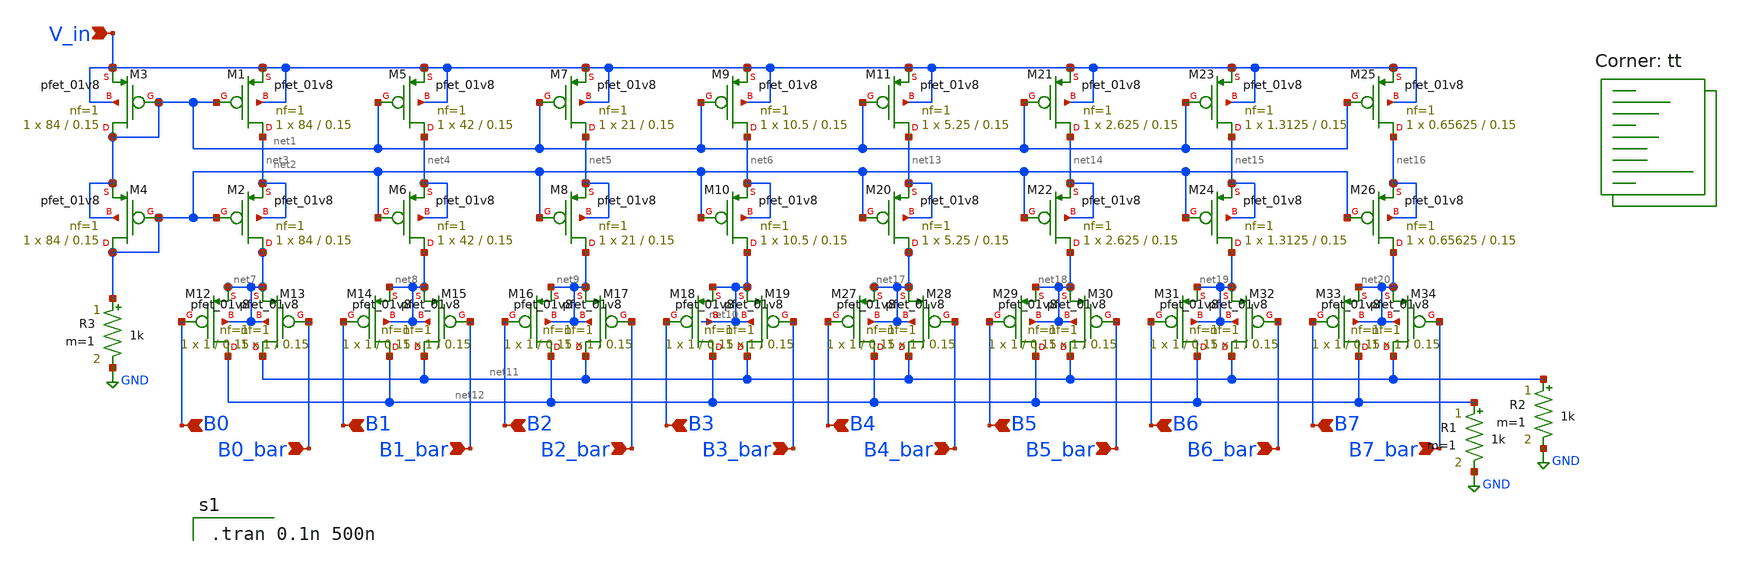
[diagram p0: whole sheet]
** sch_path: analog/schematics/DAC.sch
**.subckt DAC B0 V_in B0_bar B1 B2 B3 B1_bar B2_bar B3_bar B4 B4_bar B5 B6 B7 B5_bar B6_bar B7_bar
*.ipin B0
*.ipin V_in
*.ipin B0_bar
*.ipin B1
*.ipin B2
*.ipin B3
*.ipin B1_bar
*.ipin B2_bar
*.ipin B3_bar
*.ipin B4
*.ipin B4_bar
*.ipin B5
*.ipin B6
*.ipin B7
*.ipin B5_bar
*.ipin B6_bar
*.ipin B7_bar
XM1 net3 net1 V_in V_in sky130_fd_pr__pfet_01v8 L=0.15 W=84 nf=1 ad='int((nf+1)/2) * W/nf * 0.29' as='int((nf+2)/2) * W/nf * 0.29'
+ pd='2*int((nf+1)/2) * (W/nf + 0.29)' ps='2*int((nf+2)/2) * (W/nf + 0.29)' nrd='0.29 / W' nrs='0.29 / W'
+ sa=0 sb=0 sd=0 mult=1 m=1
XM2 net7 net2 net3 net3 sky130_fd_pr__pfet_01v8 L=0.15 W=84 nf=1 ad='int((nf+1)/2) * W/nf * 0.29' as='int((nf+2)/2) * W/nf * 0.29'
+ pd='2*int((nf+1)/2) * (W/nf + 0.29)' ps='2*int((nf+2)/2) * (W/nf + 0.29)' nrd='0.29 / W' nrs='0.29 / W'
+ sa=0 sb=0 sd=0 mult=1 m=1
XM3 net1 net1 V_in V_in sky130_fd_pr__pfet_01v8 L=0.15 W=84 nf=1 ad='int((nf+1)/2) * W/nf * 0.29' as='int((nf+2)/2) * W/nf * 0.29'
+ pd='2*int((nf+1)/2) * (W/nf + 0.29)' ps='2*int((nf+2)/2) * (W/nf + 0.29)' nrd='0.29 / W' nrs='0.29 / W'
+ sa=0 sb=0 sd=0 mult=1 m=1
XM4 net2 net2 net1 net1 sky130_fd_pr__pfet_01v8 L=0.15 W=84 nf=1 ad='int((nf+1)/2) * W/nf * 0.29' as='int((nf+2)/2) * W/nf * 0.29'
+ pd='2*int((nf+1)/2) * (W/nf + 0.29)' ps='2*int((nf+2)/2) * (W/nf + 0.29)' nrd='0.29 / W' nrs='0.29 / W'
+ sa=0 sb=0 sd=0 mult=1 m=1
XM5 net4 net1 V_in V_in sky130_fd_pr__pfet_01v8 L=0.15 W=42 nf=1 ad='int((nf+1)/2) * W/nf * 0.29' as='int((nf+2)/2) * W/nf * 0.29'
+ pd='2*int((nf+1)/2) * (W/nf + 0.29)' ps='2*int((nf+2)/2) * (W/nf + 0.29)' nrd='0.29 / W' nrs='0.29 / W'
+ sa=0 sb=0 sd=0 mult=1 m=1
XM6 net8 net2 net4 net4 sky130_fd_pr__pfet_01v8 L=0.15 W=42 nf=1 ad='int((nf+1)/2) * W/nf * 0.29' as='int((nf+2)/2) * W/nf * 0.29'
+ pd='2*int((nf+1)/2) * (W/nf + 0.29)' ps='2*int((nf+2)/2) * (W/nf + 0.29)' nrd='0.29 / W' nrs='0.29 / W'
+ sa=0 sb=0 sd=0 mult=1 m=1
XM7 net5 net1 V_in V_in sky130_fd_pr__pfet_01v8 L=0.15 W=21 nf=1 ad='int((nf+1)/2) * W/nf * 0.29' as='int((nf+2)/2) * W/nf * 0.29'
+ pd='2*int((nf+1)/2) * (W/nf + 0.29)' ps='2*int((nf+2)/2) * (W/nf + 0.29)' nrd='0.29 / W' nrs='0.29 / W'
+ sa=0 sb=0 sd=0 mult=1 m=1
XM8 net9 net2 net5 net5 sky130_fd_pr__pfet_01v8 L=0.15 W=21 nf=1 ad='int((nf+1)/2) * W/nf * 0.29' as='int((nf+2)/2) * W/nf * 0.29'
+ pd='2*int((nf+1)/2) * (W/nf + 0.29)' ps='2*int((nf+2)/2) * (W/nf + 0.29)' nrd='0.29 / W' nrs='0.29 / W'
+ sa=0 sb=0 sd=0 mult=1 m=1
XM9 net6 net1 V_in V_in sky130_fd_pr__pfet_01v8 L=0.15 W=10.5 nf=1 ad='int((nf+1)/2) * W/nf * 0.29' as='int((nf+2)/2) * W/nf * 0.29'
+ pd='2*int((nf+1)/2) * (W/nf + 0.29)' ps='2*int((nf+2)/2) * (W/nf + 0.29)' nrd='0.29 / W' nrs='0.29 / W'
+ sa=0 sb=0 sd=0 mult=1 m=1
XM10 net10 net2 net6 net6 sky130_fd_pr__pfet_01v8 L=0.15 W=10.5 nf=1 ad='int((nf+1)/2) * W/nf * 0.29'
+ as='int((nf+2)/2) * W/nf * 0.29' pd='2*int((nf+1)/2) * (W/nf + 0.29)' ps='2*int((nf+2)/2) * (W/nf + 0.29)'
+ nrd='0.29 / W' nrs='0.29 / W' sa=0 sb=0 sd=0 mult=1 m=1
XM12 net12 B0 net7 net7 sky130_fd_pr__pfet_01v8 L=0.15 W=1 nf=1 ad='int((nf+1)/2) * W/nf * 0.29' as='int((nf+2)/2) * W/nf * 0.29'
+ pd='2*int((nf+1)/2) * (W/nf + 0.29)' ps='2*int((nf+2)/2) * (W/nf + 0.29)' nrd='0.29 / W' nrs='0.29 / W'
+ sa=0 sb=0 sd=0 mult=1 m=1
XM13 net11 B0_bar net7 net7 sky130_fd_pr__pfet_01v8 L=0.15 W=1 nf=1 ad='int((nf+1)/2) * W/nf * 0.29'
+ as='int((nf+2)/2) * W/nf * 0.29' pd='2*int((nf+1)/2) * (W/nf + 0.29)' ps='2*int((nf+2)/2) * (W/nf + 0.29)'
+ nrd='0.29 / W' nrs='0.29 / W' sa=0 sb=0 sd=0 mult=1 m=1
XM14 net12 B1 net8 net8 sky130_fd_pr__pfet_01v8 L=0.15 W=1 nf=1 ad='int((nf+1)/2) * W/nf * 0.29' as='int((nf+2)/2) * W/nf * 0.29'
+ pd='2*int((nf+1)/2) * (W/nf + 0.29)' ps='2*int((nf+2)/2) * (W/nf + 0.29)' nrd='0.29 / W' nrs='0.29 / W'
+ sa=0 sb=0 sd=0 mult=1 m=1
XM15 net11 B1_bar net8 net8 sky130_fd_pr__pfet_01v8 L=0.15 W=1 nf=1 ad='int((nf+1)/2) * W/nf * 0.29'
+ as='int((nf+2)/2) * W/nf * 0.29' pd='2*int((nf+1)/2) * (W/nf + 0.29)' ps='2*int((nf+2)/2) * (W/nf + 0.29)'
+ nrd='0.29 / W' nrs='0.29 / W' sa=0 sb=0 sd=0 mult=1 m=1
XM16 net12 B2 net9 net9 sky130_fd_pr__pfet_01v8 L=0.15 W=1 nf=1 ad='int((nf+1)/2) * W/nf * 0.29' as='int((nf+2)/2) * W/nf * 0.29'
+ pd='2*int((nf+1)/2) * (W/nf + 0.29)' ps='2*int((nf+2)/2) * (W/nf + 0.29)' nrd='0.29 / W' nrs='0.29 / W'
+ sa=0 sb=0 sd=0 mult=1 m=1
XM17 net11 B2_bar net9 net9 sky130_fd_pr__pfet_01v8 L=0.15 W=1 nf=1 ad='int((nf+1)/2) * W/nf * 0.29'
+ as='int((nf+2)/2) * W/nf * 0.29' pd='2*int((nf+1)/2) * (W/nf + 0.29)' ps='2*int((nf+2)/2) * (W/nf + 0.29)'
+ nrd='0.29 / W' nrs='0.29 / W' sa=0 sb=0 sd=0 mult=1 m=1
XM18 net12 B3 net10 net10 sky130_fd_pr__pfet_01v8 L=0.15 W=1 nf=1 ad='int((nf+1)/2) * W/nf * 0.29' as='int((nf+2)/2) * W/nf * 0.29'
+ pd='2*int((nf+1)/2) * (W/nf + 0.29)' ps='2*int((nf+2)/2) * (W/nf + 0.29)' nrd='0.29 / W' nrs='0.29 / W'
+ sa=0 sb=0 sd=0 mult=1 m=1
XM19 net11 B3_bar net10 net10 sky130_fd_pr__pfet_01v8 L=0.15 W=1 nf=1 ad='int((nf+1)/2) * W/nf * 0.29'
+ as='int((nf+2)/2) * W/nf * 0.29' pd='2*int((nf+1)/2) * (W/nf + 0.29)' ps='2*int((nf+2)/2) * (W/nf + 0.29)'
+ nrd='0.29 / W' nrs='0.29 / W' sa=0 sb=0 sd=0 mult=1 m=1
XM11 net13 net1 V_in V_in sky130_fd_pr__pfet_01v8 L=0.15 W=5.25 nf=1 ad='int((nf+1)/2) * W/nf * 0.29'
+ as='int((nf+2)/2) * W/nf * 0.29' pd='2*int((nf+1)/2) * (W/nf + 0.29)' ps='2*int((nf+2)/2) * (W/nf + 0.29)'
+ nrd='0.29 / W' nrs='0.29 / W' sa=0 sb=0 sd=0 mult=1 m=1
XM20 net17 net2 net13 net13 sky130_fd_pr__pfet_01v8 L=0.15 W=5.25 nf=1 ad='int((nf+1)/2) * W/nf * 0.29'
+ as='int((nf+2)/2) * W/nf * 0.29' pd='2*int((nf+1)/2) * (W/nf + 0.29)' ps='2*int((nf+2)/2) * (W/nf + 0.29)'
+ nrd='0.29 / W' nrs='0.29 / W' sa=0 sb=0 sd=0 mult=1 m=1
XM21 net14 net1 V_in V_in sky130_fd_pr__pfet_01v8 L=0.15 W=2.625 nf=1 ad='int((nf+1)/2) * W/nf * 0.29'
+ as='int((nf+2)/2) * W/nf * 0.29' pd='2*int((nf+1)/2) * (W/nf + 0.29)' ps='2*int((nf+2)/2) * (W/nf + 0.29)'
+ nrd='0.29 / W' nrs='0.29 / W' sa=0 sb=0 sd=0 mult=1 m=1
XM22 net18 net2 net14 net14 sky130_fd_pr__pfet_01v8 L=0.15 W=2.625 nf=1 ad='int((nf+1)/2) * W/nf * 0.29'
+ as='int((nf+2)/2) * W/nf * 0.29' pd='2*int((nf+1)/2) * (W/nf + 0.29)' ps='2*int((nf+2)/2) * (W/nf + 0.29)'
+ nrd='0.29 / W' nrs='0.29 / W' sa=0 sb=0 sd=0 mult=1 m=1
XM23 net15 net1 V_in V_in sky130_fd_pr__pfet_01v8 L=0.15 W=1.3125 nf=1 ad='int((nf+1)/2) * W/nf * 0.29'
+ as='int((nf+2)/2) * W/nf * 0.29' pd='2*int((nf+1)/2) * (W/nf + 0.29)' ps='2*int((nf+2)/2) * (W/nf + 0.29)'
+ nrd='0.29 / W' nrs='0.29 / W' sa=0 sb=0 sd=0 mult=1 m=1
XM24 net19 net2 net15 net15 sky130_fd_pr__pfet_01v8 L=0.15 W=1.3125 nf=1 ad='int((nf+1)/2) * W/nf * 0.29'
+ as='int((nf+2)/2) * W/nf * 0.29' pd='2*int((nf+1)/2) * (W/nf + 0.29)' ps='2*int((nf+2)/2) * (W/nf + 0.29)'
+ nrd='0.29 / W' nrs='0.29 / W' sa=0 sb=0 sd=0 mult=1 m=1
XM25 net16 net1 V_in V_in sky130_fd_pr__pfet_01v8 L=0.15 W=0.65625 nf=1 ad='int((nf+1)/2) * W/nf * 0.29'
+ as='int((nf+2)/2) * W/nf * 0.29' pd='2*int((nf+1)/2) * (W/nf + 0.29)' ps='2*int((nf+2)/2) * (W/nf + 0.29)'
+ nrd='0.29 / W' nrs='0.29 / W' sa=0 sb=0 sd=0 mult=1 m=1
XM26 net20 net2 net16 net16 sky130_fd_pr__pfet_01v8 L=0.15 W=0.65625 nf=1 ad='int((nf+1)/2) * W/nf * 0.29'
+ as='int((nf+2)/2) * W/nf * 0.29' pd='2*int((nf+1)/2) * (W/nf + 0.29)' ps='2*int((nf+2)/2) * (W/nf + 0.29)'
+ nrd='0.29 / W' nrs='0.29 / W' sa=0 sb=0 sd=0 mult=1 m=1
XM27 net12 B4 net17 net17 sky130_fd_pr__pfet_01v8 L=0.15 W=1 nf=1 ad='int((nf+1)/2) * W/nf * 0.29' as='int((nf+2)/2) * W/nf * 0.29'
+ pd='2*int((nf+1)/2) * (W/nf + 0.29)' ps='2*int((nf+2)/2) * (W/nf + 0.29)' nrd='0.29 / W' nrs='0.29 / W'
+ sa=0 sb=0 sd=0 mult=1 m=1
XM28 net11 B4_bar net17 net17 sky130_fd_pr__pfet_01v8 L=0.15 W=1 nf=1 ad='int((nf+1)/2) * W/nf * 0.29'
+ as='int((nf+2)/2) * W/nf * 0.29' pd='2*int((nf+1)/2) * (W/nf + 0.29)' ps='2*int((nf+2)/2) * (W/nf + 0.29)'
+ nrd='0.29 / W' nrs='0.29 / W' sa=0 sb=0 sd=0 mult=1 m=1
XM29 net12 B5 net18 net18 sky130_fd_pr__pfet_01v8 L=0.15 W=1 nf=1 ad='int((nf+1)/2) * W/nf * 0.29' as='int((nf+2)/2) * W/nf * 0.29'
+ pd='2*int((nf+1)/2) * (W/nf + 0.29)' ps='2*int((nf+2)/2) * (W/nf + 0.29)' nrd='0.29 / W' nrs='0.29 / W'
+ sa=0 sb=0 sd=0 mult=1 m=1
XM30 net11 B5_bar net18 net18 sky130_fd_pr__pfet_01v8 L=0.15 W=1 nf=1 ad='int((nf+1)/2) * W/nf * 0.29'
+ as='int((nf+2)/2) * W/nf * 0.29' pd='2*int((nf+1)/2) * (W/nf + 0.29)' ps='2*int((nf+2)/2) * (W/nf + 0.29)'
+ nrd='0.29 / W' nrs='0.29 / W' sa=0 sb=0 sd=0 mult=1 m=1
XM31 net12 B6 net19 net19 sky130_fd_pr__pfet_01v8 L=0.15 W=1 nf=1 ad='int((nf+1)/2) * W/nf * 0.29' as='int((nf+2)/2) * W/nf * 0.29'
+ pd='2*int((nf+1)/2) * (W/nf + 0.29)' ps='2*int((nf+2)/2) * (W/nf + 0.29)' nrd='0.29 / W' nrs='0.29 / W'
+ sa=0 sb=0 sd=0 mult=1 m=1
XM32 net11 B6_bar net19 net19 sky130_fd_pr__pfet_01v8 L=0.15 W=1 nf=1 ad='int((nf+1)/2) * W/nf * 0.29'
+ as='int((nf+2)/2) * W/nf * 0.29' pd='2*int((nf+1)/2) * (W/nf + 0.29)' ps='2*int((nf+2)/2) * (W/nf + 0.29)'
+ nrd='0.29 / W' nrs='0.29 / W' sa=0 sb=0 sd=0 mult=1 m=1
XM33 net12 B7 net20 net20 sky130_fd_pr__pfet_01v8 L=0.15 W=1 nf=1 ad='int((nf+1)/2) * W/nf * 0.29' as='int((nf+2)/2) * W/nf * 0.29'
+ pd='2*int((nf+1)/2) * (W/nf + 0.29)' ps='2*int((nf+2)/2) * (W/nf + 0.29)' nrd='0.29 / W' nrs='0.29 / W'
+ sa=0 sb=0 sd=0 mult=1 m=1
XM34 net11 B7_bar net20 net20 sky130_fd_pr__pfet_01v8 L=0.15 W=1 nf=1 ad='int((nf+1)/2) * W/nf * 0.29'
+ as='int((nf+2)/2) * W/nf * 0.29' pd='2*int((nf+1)/2) * (W/nf + 0.29)' ps='2*int((nf+2)/2) * (W/nf + 0.29)'
+ nrd='0.29 / W' nrs='0.29 / W' sa=0 sb=0 sd=0 mult=1 m=1
R1 net12 GND 1k m=1
R2 net11 GND 1k m=1
R3 net2 GND 1k m=1
**** begin user architecture code
.lib $::SKYWATER_MODELS/sky130.lib.spice tt

.tran 0.1n 500n

**** end user architecture code
**.ends
.GLOBAL GND
.end
